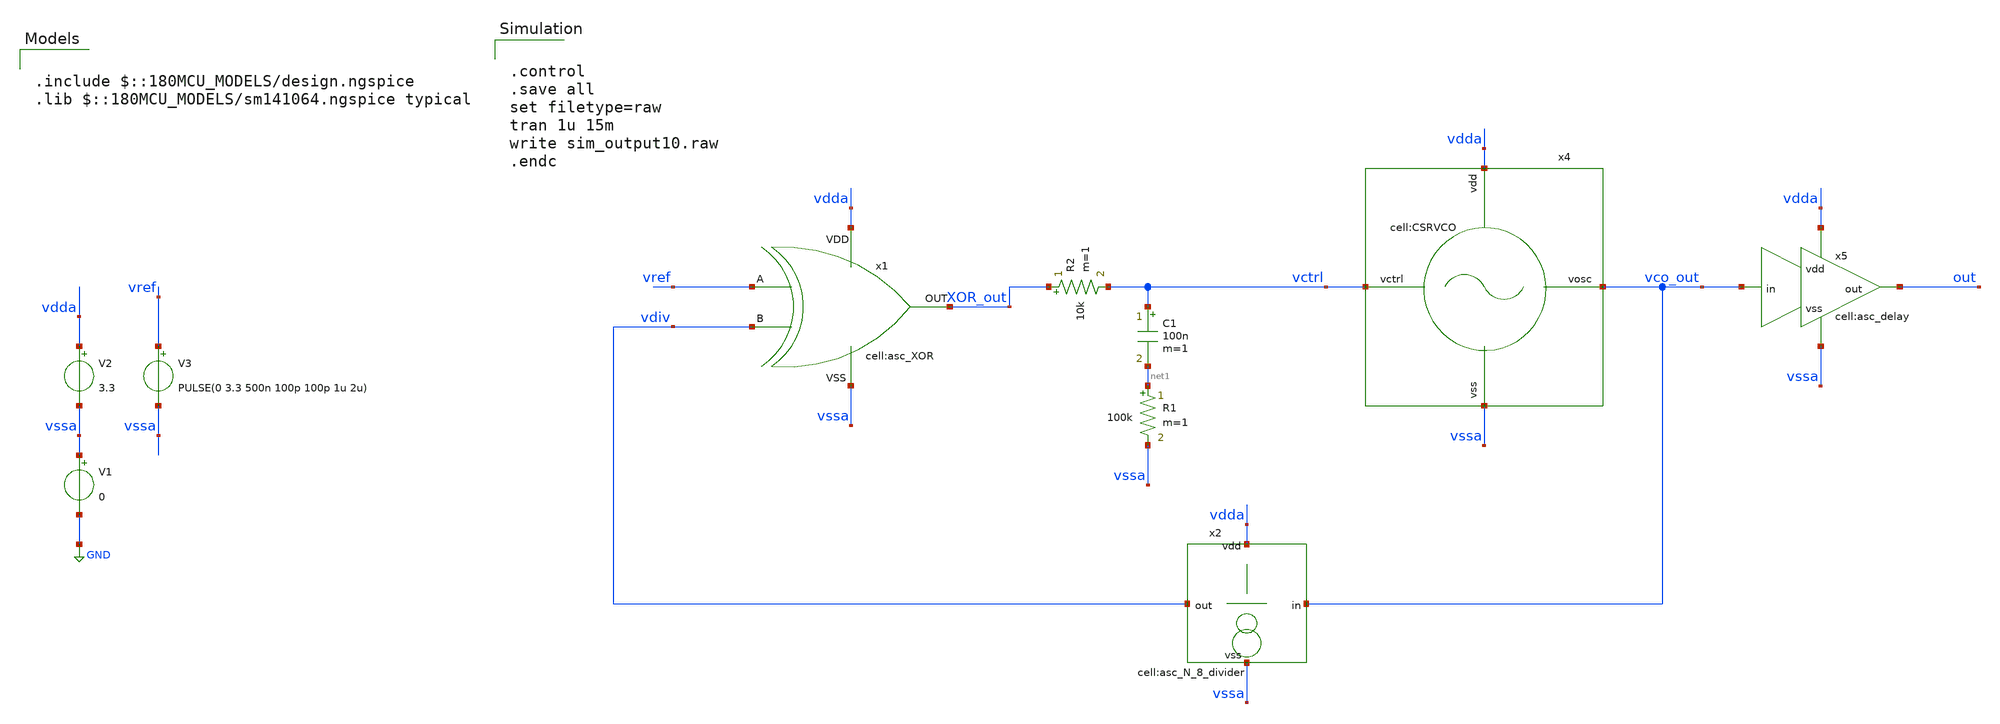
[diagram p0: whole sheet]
** sch_path: designs/libs/tb_analog/tb_xor_pll/tb_xor_pll.sch
**.subckt tb_xor_pll
V1 vssa GND 0
V2 vdda vssa 3.3
V3 vref vssa PULSE(0 3.3 500n 100p 100p 1u 2u)
x4 vctrl vdda vssa vco_out CSRVCO
x5 vco_out vssa out vdda asc_delay
C1 vctrl net1 100n m=1
x1 vdda vssa XOR_out vref vdiv asc_XOR
x2 vco_out vdiv vdda vssa asc_N_8_divider
R2 XOR_out vctrl 10k m=1
R1 net1 vssa 100k m=1
**** begin user architecture code

.include $::180MCU_MODELS/design.ngspice
.lib $::180MCU_MODELS/sm141064.ngspice typical



.control
.save all
set filetype=raw
tran 1u 15m
write sim_output10.raw
.endc


**** end user architecture code
**.ends
.GLOBAL GND
.end
